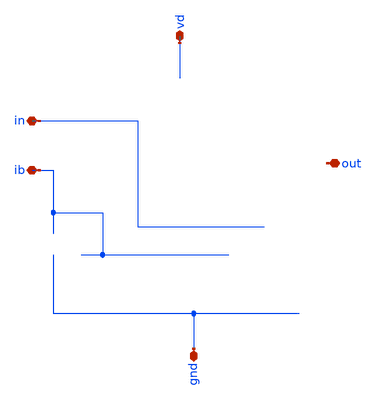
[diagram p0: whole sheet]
** sch_path: buffer/xschem/buffer-pex.sch
* Copyright 2020 Stefan Frederik Schippers
* Licensed under the Apache License, Version 2.0 (the "License");
* you may not use this file except in compliance with the License.
* You may obtain a copy of the License at
* https://www.apache.org/licenses/LICENSE-2.0
* Unless required by applicable law or agreed to in writing, software
* distributed under the License is distributed on an "AS IS" BASIS,
* WITHOUT WARRANTIES OR CONDITIONS OF ANY KIND, either express or implied.
* See the License for the specific language governing permissions and
* limitations under the License.
**.subckt buffer-pex vd ib out in gnd
*.iopin vd
*.iopin ib
*.iopin out
*.iopin in
*.iopin gnd
**** begin user architecture code


* NGSPICE file created from buffer.ext - technology: sky130A

*.subckt buffer vd ib out in gnd
X0 out.t19 net1.t27 gnd.t45 gnd.t7 sky130_fd_pr__nfet_01v8 ad=0.145 pd=1.29 as=0.145 ps=1.29 w=1 l=1
X1 a_19996_3619# a_19796_3522# a_19738_3619# w_19600_3400# sky130_fd_pr__pfet_01v8 ad=0.29 pd=2.58
+ as=0.29 ps=2.58 w=1 l=1
X2 net2.t11 out.t20 net4.t20 gnd.t8 sky130_fd_pr__nfet_01v8 ad=0.145 pd=1.29 as=0.145 ps=1.29 w=1
+ l=1
X3 gnd.t44 net1.t10 net1 gnd.t9 sky130_fd_pr__nfet_01v8 ad=0.145 pd=1.29 as=0.145 ps=1.29 w=1 l=1
X4 net4.t10 in.t0 net3.t11 gnd.t24 sky130_fd_pr__nfet_01v8 ad=0.145 pd=1.29 as=0.145 ps=1.29 w=1 l=1
X5 net3.t1 net3.t0 vd.t21 vd.t20 sky130_fd_pr__pfet_01v8 ad=0.29 pd=2.58 as=0.29 ps=2.58 w=1 l=1
X6 vd.t19 net3.t12 out.t7 vd.t18 sky130_fd_pr__pfet_01v8 ad=0.145 pd=1.29 as=0.29 ps=2.58 w=1 l=1
X7 a_14516_4519# a_14316_4422# a_14258_4519# w_14120_4300# sky130_fd_pr__pfet_01v8 ad=0.29 pd=2.58
+ as=0.29 ps=2.58 w=1 l=1
X8 a_15696_2770# a_15496_2682# a_15438_2770# gnd.t46 sky130_fd_pr__nfet_01v8 ad=0.29 pd=2.58 as=0.29
+ ps=2.58 w=1 l=1
X9 net1.t0 net2.t12 vd.t43 vd.t42 sky130_fd_pr__pfet_01v8 ad=0.145 pd=1.29 as=0.145 ps=1.29 w=1 l=1
X10 net4.t9 in.t1 net3.t10 gnd.t23 sky130_fd_pr__nfet_01v8 ad=0.145 pd=1.29 as=0.29 ps=2.58 w=1 l=1
X11 net2.t10 out.t21 net4.t18 gnd.t5 sky130_fd_pr__nfet_01v8 ad=0.145 pd=1.29 as=0.145 ps=1.29 w=1
+ l=1
X12 gnd.t43 net1.t11 net1 gnd.t8 sky130_fd_pr__nfet_01v8 ad=0.145 pd=1.29 as=0.145 ps=1.29 w=1 l=1
X13 out.t22 net1.t6 sky130_fd_pr__cap_mim_m3_2 l=21 w=21
X14 net1 net1.t19 gnd.t42 gnd.t24 sky130_fd_pr__nfet_01v8 ad=0.145 pd=1.29 as=0.145 ps=1.29 w=1 l=1
X15 gnd.t41 net1.t15 net1.t16 gnd.t5 sky130_fd_pr__nfet_01v8 ad=0.145 pd=1.29 as=0.145 ps=1.29 w=1
+ l=1
X16 a_19996_4519# a_19796_4422# a_19738_4519# w_19600_4300# sky130_fd_pr__pfet_01v8 ad=0.29 pd=2.58
+ as=0.29 ps=2.58 w=1 l=1
X17 net4.t11 out.t23 net2.t9 gnd.t14 sky130_fd_pr__nfet_01v8 ad=0.145 pd=1.29 as=0.145 ps=1.29 w=1
+ l=1
X18 a_14756_1890# a_14556_1802# a_14498_1890# gnd.t1 sky130_fd_pr__nfet_01v8 ad=0.29 pd=2.58 as=0.29
+ ps=2.58 w=1 l=1
X19 net1.t13 net1.t12 gnd.t40 gnd.t23 sky130_fd_pr__nfet_01v8 ad=0.145 pd=1.29 as=0.29 ps=2.58 w=1
+ l=1
X20 net3.t9 in.t2 net4.t8 gnd.t22 sky130_fd_pr__nfet_01v8 ad=0.145 pd=1.29 as=0.145 ps=1.29 w=1 l=1
X21 net3.t8 in.t3 net4.t7 gnd.t21 sky130_fd_pr__nfet_01v8 ad=0.29 pd=2.58 as=0.145 ps=1.29 w=1 l=1
X22 net2.t1 net2.t0 vd.t41 vd.t40 sky130_fd_pr__pfet_01v8 ad=0.29 pd=2.58 as=0.29 ps=2.58 w=1 l=1
X23 vd.t39 net2.t13 net1.t8 vd.t38 sky130_fd_pr__pfet_01v8 ad=0.145 pd=1.29 as=0.29 ps=2.58 w=1 l=1
X24 net4.t14 out.t24 net2.t8 gnd.t11 sky130_fd_pr__nfet_01v8 ad=0.145 pd=1.29 as=0.145 ps=1.29 w=1
+ l=1
X25 net4.t15 out.t25 net2.t7 gnd.t6 sky130_fd_pr__nfet_01v8 ad=0.145 pd=1.29 as=0.145 ps=1.29 w=1
+ l=1
X26 out.t18 net1.t28 gnd.t39 gnd.t14 sky130_fd_pr__nfet_01v8 ad=0.145 pd=1.29 as=0.145 ps=1.29 w=1
+ l=1
X27 vd.t17 net3.t13 out.t9 vd.t16 sky130_fd_pr__pfet_01v8 ad=0.145 pd=1.29 as=0.145 ps=1.29 w=1 l=1
X28 net2.t6 out.t26 net4.t19 gnd.t10 sky130_fd_pr__nfet_01v8 ad=0.145 pd=1.29 as=0.145 ps=1.29 w=1
+ l=1
X29 out.t1 net3.t14 vd.t15 vd.t14 sky130_fd_pr__pfet_01v8 ad=0.145 pd=1.29 as=0.29 ps=2.58 w=1 l=1
X30 net4.t6 in.t4 net3.t7 gnd.t20 sky130_fd_pr__nfet_01v8 ad=0.145 pd=1.29 as=0.145 ps=1.29 w=1 l=1
X31 gnd.t26 net1.t29 out.t17 gnd.t21 sky130_fd_pr__nfet_01v8 ad=0.29 pd=2.58 as=0.145 ps=1.29 w=1
+ l=1
X32 gnd.t38 net1.t30 out.t16 gnd.t22 sky130_fd_pr__nfet_01v8 ad=0.145 pd=1.29 as=0.145 ps=1.29 w=1
+ l=1
X33 gnd.t37 net1.t24 net1.t25 gnd.t10 sky130_fd_pr__nfet_01v8 ad=0.145 pd=1.29 as=0.145 ps=1.29 w=1
+ l=1
X34 out.t15 net1.t31 gnd.t28 gnd.t11 sky130_fd_pr__nfet_01v8 ad=0.145 pd=1.29 as=0.145 ps=1.29 w=1
+ l=1
X35 out.t14 net1.t32 gnd.t36 gnd.t6 sky130_fd_pr__nfet_01v8 ad=0.145 pd=1.29 as=0.145 ps=1.29 w=1
+ l=1
X36 net1.t23 net1.t22 gnd.t35 gnd.t20 sky130_fd_pr__nfet_01v8 ad=0.145 pd=1.29 as=0.145 ps=1.29 w=1
+ l=1
X37 gnd.t13 ib.t0 ib.t1 gnd.t12 sky130_fd_pr__nfet_01v8 ad=0.145 pd=1.29 as=0.29 ps=2.58 w=1 l=1
X38 net4.t0 ib.t2 gnd.t3 gnd.t2 sky130_fd_pr__nfet_01v8 ad=0.29 pd=2.58 as=0.145 ps=1.29 w=1 l=1
X39 vd.t13 net3.t15 out.t8 vd.t12 sky130_fd_pr__pfet_01v8 ad=0.29 pd=2.58 as=0.145 ps=1.29 w=1 l=1
X40 net3.t6 in.t5 net4.t5 gnd.t19 sky130_fd_pr__nfet_01v8 ad=0.145 pd=1.29 as=0.145 ps=1.29 w=1 l=1
X41 vd.t11 net3.t16 out.t6 vd.t10 sky130_fd_pr__pfet_01v8 ad=0.145 pd=1.29 as=0.145 ps=1.29 w=1 l=1
X42 net4.t16 out.t27 net2.t5 gnd.t0 sky130_fd_pr__nfet_01v8 ad=0.145 pd=1.29 as=0.145 ps=1.29 w=1
+ l=1
X43 out.t0 net3.t17 vd.t9 vd.t8 sky130_fd_pr__pfet_01v8 ad=0.145 pd=1.29 as=0.145 ps=1.29 w=1 l=1
X44 vd.t7 net3.t18 out.t3 vd.t6 sky130_fd_pr__pfet_01v8 ad=0.145 pd=1.29 as=0.145 ps=1.29 w=1 l=1
X45 net4.t4 in.t6 net3.t5 gnd.t18 sky130_fd_pr__nfet_01v8 ad=0.145 pd=1.29 as=0.145 ps=1.29 w=1 l=1
X46 net2.t4 out.t28 net4.t12 gnd.t33 sky130_fd_pr__nfet_01v8 ad=0.145 pd=1.29 as=0.145 ps=1.29 w=1
+ l=1
X47 vd.t37 net2.t14 net1.t26 vd.t36 sky130_fd_pr__pfet_01v8 ad=0.145 pd=1.29 as=0.145 ps=1.29 w=1
+ l=1
X48 out.t5 net3.t19 vd.t5 vd.t4 sky130_fd_pr__pfet_01v8 ad=0.29 pd=2.58 as=0.145 ps=1.29 w=1 l=1
X49 out.t2 net3.t20 vd.t3 vd.t2 sky130_fd_pr__pfet_01v8 ad=0.145 pd=1.29 as=0.145 ps=1.29 w=1 l=1
X50 net4.t3 in.t7 net3.t4 gnd.t17 sky130_fd_pr__nfet_01v8 ad=0.145 pd=1.29 as=0.145 ps=1.29 w=1 l=1
X51 net1.t7 net2.t15 vd.t35 vd.t34 sky130_fd_pr__pfet_01v8 ad=0.145 pd=1.29 as=0.29 ps=2.58 w=1 l=1
X52 gnd.t27 net1.t33 out.t13 gnd.t19 sky130_fd_pr__nfet_01v8 ad=0.145 pd=1.29 as=0.145 ps=1.29 w=1
+ l=1
X53 gnd.t34 net1.t20 net1.t21 gnd.t33 sky130_fd_pr__nfet_01v8 ad=0.145 pd=1.29 as=0.145 ps=1.29 w=1
+ l=1
X54 out.t12 net1.t34 gnd.t32 gnd.t0 sky130_fd_pr__nfet_01v8 ad=0.145 pd=1.29 as=0.145 ps=1.29 w=1
+ l=1
X55 a_21836_2770# a_21636_2682# a_21578_2770# gnd.t4 sky130_fd_pr__nfet_01v8 ad=0.29 pd=2.58 as=0.29
+ ps=2.58 w=1 l=1
X56 net1.t18 net1.t17 gnd.t31 gnd.t18 sky130_fd_pr__nfet_01v8 ad=0.145 pd=1.29 as=0.145 ps=1.29 w=1
+ l=1
X57 net1 net1.t14 gnd.t30 gnd.t17 sky130_fd_pr__nfet_01v8 ad=0.145 pd=1.29 as=0.145 ps=1.29 w=1 l=1
X58 a_14516_3619# a_14316_3522# a_14258_3619# w_14120_3400# sky130_fd_pr__pfet_01v8 ad=0.29 pd=2.58
+ as=0.29 ps=2.58 w=1 l=1
X59 net3.t3 in.t8 net4.t2 gnd.t16 sky130_fd_pr__nfet_01v8 ad=0.145 pd=1.29 as=0.145 ps=1.29 w=1 l=1
X60 net3.t2 in.t9 net4.t1 gnd.t15 sky130_fd_pr__nfet_01v8 ad=0.145 pd=1.29 as=0.145 ps=1.29 w=1 l=1
X61 vd.t33 net2.t16 net1.t3 vd.t32 sky130_fd_pr__pfet_01v8 ad=0.29 pd=2.58 as=0.145 ps=1.29 w=1 l=1
X62 out.t4 net3.t21 vd.t1 vd.t0 sky130_fd_pr__pfet_01v8 ad=0.145 pd=1.29 as=0.145 ps=1.29 w=1 l=1
X63 net4.t17 out.t29 net2.t3 gnd.t7 sky130_fd_pr__nfet_01v8 ad=0.145 pd=1.29 as=0.145 ps=1.29 w=1
+ l=1
X64 vd.t31 net2.t17 net1.t4 vd.t30 sky130_fd_pr__pfet_01v8 ad=0.145 pd=1.29 as=0.145 ps=1.29 w=1 l=1
X65 net2.t2 out.t30 net4.t13 gnd.t9 sky130_fd_pr__nfet_01v8 ad=0.145 pd=1.29 as=0.145 ps=1.29 w=1
+ l=1
X66 a_21836_1890# a_21636_1802# a_21578_1890# gnd.t4 sky130_fd_pr__nfet_01v8 ad=0.29 pd=2.58 as=0.29
+ ps=2.58 w=1 l=1
X67 net1.t1 net2.t18 vd.t29 vd.t28 sky130_fd_pr__pfet_01v8 ad=0.145 pd=1.29 as=0.145 ps=1.29 w=1 l=1
X68 net1.t5 net2.t19 vd.t27 vd.t26 sky130_fd_pr__pfet_01v8 ad=0.145 pd=1.29 as=0.145 ps=1.29 w=1 l=1
X69 vd.t25 net2.t20 net1.t2 vd.t24 sky130_fd_pr__pfet_01v8 ad=0.145 pd=1.29 as=0.145 ps=1.29 w=1 l=1
X70 net1.t9 net2.t21 vd.t23 vd.t22 sky130_fd_pr__pfet_01v8 ad=0.29 pd=2.58 as=0.145 ps=1.29 w=1 l=1
X71 gnd.t29 net1.t35 out.t11 gnd.t16 sky130_fd_pr__nfet_01v8 ad=0.145 pd=1.29 as=0.145 ps=1.29 w=1
+ l=1
X72 gnd.t25 net1.t36 out.t10 gnd.t15 sky130_fd_pr__nfet_01v8 ad=0.145 pd=1.29 as=0.145 ps=1.29 w=1
+ l=1
R0 net1.n12 net1.t29 172.22
R1 net1.n13 net1.n12 149.524
R2 net1.n14 net1.n13 149.524
R3 net1.n15 net1.n14 149.524
R4 net1.n16 net1.n15 149.524
R5 net1.n17 net1.n16 149.524
R6 net1.n18 net1.n17 149.524
R7 net1.n19 net1.n18 149.524
R8 net1.n20 net1.n19 149.524
R9 net1.n21 net1.n20 149.524
R10 net1.n22 net1.n21 149.524
R11 net1.n23 net1.n22 149.524
R12 net1.n24 net1.n23 149.524
R13 net1.n25 net1.n24 149.524
R14 net1.n26 net1.n25 149.524
R15 net1.n27 net1.n26 149.524
R16 net1.n28 net1.n27 149.524
R17 net1.n29 net1.n28 149.524
R18 net1.n1 net1.n29 148.639
R19 net1.n10 net1.t9 28.7308
R20 net1.n8 net1.t8 28.7308
R21 net1.n9 net1.t26 28.5655
R22 net1.n9 net1.t7 28.5655
R23 net1.n3 net1.t4 28.5655
R24 net1.n3 net1.t1 28.5655
R25 net1.n7 net1.t3 28.5655
R26 net1.n7 net1.t0 28.5655
R27 net1.n4 net1.t2 28.5655
R28 net1.n4 net1.t5 28.5655
R29 net1.n1 net1.t12 24.2846
R30 net1.n29 net1.t24 24.1012
R31 net1.n28 net1.t31 24.1012
R32 net1.n27 net1.t33 24.1012
R33 net1.n26 net1.t17 24.1012
R34 net1.n25 net1.t20 24.1012
R35 net1.n24 net1.t27 24.1012
R36 net1.n23 net1.t35 24.1012
R37 net1.n22 net1.t22 24.1012
R38 net1.n21 net1.t15 24.1012
R39 net1.n20 net1.t32 24.1012
R40 net1.n19 net1.t30 24.1012
R41 net1.n18 net1.t14 24.1012
R42 net1.n17 net1.t10 24.1012
R43 net1.n16 net1.t34 24.1012
R44 net1.n15 net1.t36 24.1012
R45 net1.n14 net1.t19 24.1012
R46 net1.n13 net1.t11 24.1012
R47 net1.n12 net1.t28 24.1012
R48 net1.n2 net1.t25 17.4005
R49 net1.n2 net1.t13 17.4005
R50 net1.n5 net1.t16 17.4005
R51 net1.n5 net1.t23 17.4005
R52 net1.n6 net1.t21 17.4005
R53 net1.n6 net1.t18 17.4005
R54 net1.n30 net1.n0 3.21925
R55 net1 net1.n30 3.21925
R56 net1.n0 net1.n2 2.85119
R57 net1.n3 net1.n9 2.12411
R58 net1.n4 net1.n7 2.12411
R59 net1.n8 net1.n4 2.12411
R60 net1.n10 net1.n3 2.12411
R61 net1.n2 net1.t6 1.82437
R62 net1.n0 net1.n11 1.56782
R63 net1.n0 net1.n6 1.56492
R64 net1.n2 net1.n1 1.52493
R65 net1.n11 net1.n8 1.00578
R66 net1.n11 net1.n10 0.942223
R67 net1.n30 net1.n5 0.932973
R68 gnd.n3 gnd.n2 12625.4
R69 gnd.n71 gnd.n63 12625.4
R70 gnd.n29 gnd.n28 10965.6
R71 gnd.t11 gnd.n1 10965.6
R72 gnd.n33 gnd.n5 1104.56
R73 gnd.n32 gnd.n27 1104.56
R74 gnd.n33 gnd.n32 1104.56
R75 gnd.n41 gnd.n36 1104.56
R76 gnd.n40 gnd.n38 1104.56
R77 gnd.n41 gnd.n40 1104.56
R78 gnd.t21 gnd.t14 171.897
R79 gnd.t24 gnd.t8 171.897
R80 gnd.t15 gnd.t24 171.897
R81 gnd.t0 gnd.t15 171.897
R82 gnd.t9 gnd.t0 171.897
R83 gnd.t22 gnd.t17 171.897
R84 gnd.t6 gnd.t22 171.897
R85 gnd.t5 gnd.t20 171.897
R86 gnd.t7 gnd.t16 171.897
R87 gnd.t18 gnd.t33 171.897
R88 gnd.t19 gnd.t18 171.897
R89 gnd.t11 gnd.t19 171.897
R90 gnd.t10 gnd.t11 171.897
R91 gnd.t23 gnd.t10 171.897
R92 gnd.t4 gnd.n10 161.903
R93 gnd.n23 gnd.t4 161.903
R94 gnd.n43 gnd.t23 161.903
R95 gnd.t1 gnd.n68 161.903
R96 gnd.n25 gnd.n24 136.584
R97 gnd.n71 gnd.t1 126.591
R98 gnd.n3 gnd.t7 118.596
R99 gnd.n62 gnd.n49 109.317
R100 gnd.n78 gnd.n77 108.424
R101 gnd.t17 gnd.n29 106.603
R102 gnd.n46 gnd.n43 89.2797
R103 gnd.n75 gnd.n74 89.2797
R104 gnd.n25 gnd.n23 87.9472
R105 gnd.n30 gnd.t6 85.9484
R106 gnd.n30 gnd.t5 85.9484
R107 gnd.n59 gnd.t2 85.9484
R108 gnd.n29 gnd.t9 65.2943
R109 gnd.t33 gnd.n3 53.3015
R110 gnd.n56 gnd.t12 51.3027
R111 gnd.n47 gnd.n46 41.3088
R112 gnd.t2 gnd.t46 41.3088
R113 gnd.n74 gnd.n71 35.3124
R114 gnd.n59 gnd.n56 34.6462
R115 gnd.n24 gnd.t21 25.3185
R116 gnd.n85 gnd.t26 20.261
R117 gnd.n98 gnd.t40 17.405
R118 gnd.n0 gnd.t3 17.4005
R119 gnd.n0 gnd.t13 17.4005
R120 gnd.n80 gnd.t28 17.4005
R121 gnd.n80 gnd.t37 17.4005
R122 gnd.n95 gnd.t31 17.4005
R123 gnd.n95 gnd.t27 17.4005
R124 gnd.n81 gnd.t45 17.4005
R125 gnd.n81 gnd.t34 17.4005
R126 gnd.n92 gnd.t35 17.4005
R127 gnd.n92 gnd.t29 17.4005
R128 gnd.n82 gnd.t36 17.4005
R129 gnd.n82 gnd.t41 17.4005
R130 gnd.n89 gnd.t30 17.4005
R131 gnd.n89 gnd.t38 17.4005
R132 gnd.n83 gnd.t32 17.4005
R133 gnd.n83 gnd.t44 17.4005
R134 gnd.n86 gnd.t42 17.4005
R135 gnd.n86 gnd.t25 17.4005
R136 gnd.n84 gnd.t39 17.4005
R137 gnd.n84 gnd.t43 17.4005
R138 gnd.n90 gnd.n88 2.91898
R139 gnd.n93 gnd.n91 2.91898
R140 gnd.n96 gnd.n94 2.90766
R141 gnd.n87 gnd.n85 2.90766
R142 gnd.n98 gnd.n97 2.89724
R143 gnd.n91 gnd.n90 2.88773
R144 gnd.n97 gnd.n96 2.85648
R145 gnd.n88 gnd.n87 2.81391
R146 gnd.n94 gnd.n93 2.81391
R147 gnd gnd.n98 1.09175
R148 gnd gnd.n79 1.063
R149 gnd.n79 gnd.n78 0.884538
R150 gnd.n79 gnd.n0 0.68415
R151 gnd.n16 gnd.n15 0.0464978
R152 gnd.t4 gnd.n16 0.0464978
R153 gnd.n14 gnd.n13 0.0464978
R154 gnd.t4 gnd.n14 0.0464978
R155 gnd.n65 gnd.n64 0.0464978
R156 gnd.t1 gnd.n65 0.0464978
R157 gnd.n70 gnd.n69 0.0464978
R158 gnd.t1 gnd.n70 0.0464978
R159 gnd.n12 gnd.n11 0.0464978
R160 gnd.t4 gnd.n12 0.0464978
R161 gnd.n18 gnd.n17 0.0464978
R162 gnd.t4 gnd.n18 0.0464978
R163 gnd.n51 gnd.n50 0.0464978
R164 gnd.t46 gnd.n51 0.0464978
R165 gnd.n53 gnd.n52 0.0464978
R166 gnd.t46 gnd.n53 0.0464978
R167 gnd.n22 gnd.n21 0.0425017
R168 gnd.n23 gnd.n22 0.0425017
R169 gnd.n7 gnd.n6 0.0425017
R170 gnd.n10 gnd.n7 0.0425017
R171 gnd.n42 gnd.n41 0.0425017
R172 gnd.n43 gnd.n42 0.0425017
R173 gnd.n38 gnd.n37 0.0425017
R174 gnd.n67 gnd.n66 0.0425017
R175 gnd.n68 gnd.n67 0.0425017
R176 gnd.n73 gnd.n72 0.0425017
R177 gnd.n74 gnd.n73 0.0425017
R178 gnd.n20 gnd.n19 0.0425017
R179 gnd.n23 gnd.n20 0.0425017
R180 gnd.n9 gnd.n8 0.0425017
R181 gnd.n10 gnd.n9 0.0425017
R182 gnd.n34 gnd.n33 0.0425017
R183 gnd.n43 gnd.n34 0.0425017
R184 gnd.n27 gnd.n26 0.0425017
R185 gnd.n26 gnd.n25 0.0425017
R186 gnd.n55 gnd.n54 0.0425017
R187 gnd.n56 gnd.n55 0.0425017
R188 gnd.n45 gnd.n44 0.0425017
R189 gnd.n46 gnd.n45 0.0425017
R190 gnd.n49 gnd.n48 0.0425017
R191 gnd.n48 gnd.n47 0.0425017
R192 gnd.n77 gnd.n76 0.0425017
R193 gnd.n76 gnd.n75 0.0425017
R194 gnd.n58 gnd.n57 0.0250016
R195 gnd.n59 gnd.n58 0.0250016
R196 gnd.n79 gnd.n62 0.0147449
R197 gnd.n97 gnd.n80 0.00498379
R198 gnd.n96 gnd.n95 0.00498379
R199 gnd.n94 gnd.n81 0.00498379
R200 gnd.n93 gnd.n92 0.00498379
R201 gnd.n91 gnd.n82 0.00498379
R202 gnd.n90 gnd.n89 0.00498379
R203 gnd.n88 gnd.n83 0.00498379
R204 gnd.n87 gnd.n86 0.00498379
R205 gnd.n85 gnd.n84 0.00498379
R206 gnd.n40 gnd.n39 0.00310298
R207 gnd.n36 gnd.n35 0.00310298
R208 gnd.n32 gnd.n31 0.00310298
R209 gnd.n31 gnd.n30 0.00310298
R210 gnd.n5 gnd.n4 0.00310298
R211 gnd.n62 gnd.n61 0.00137759
R212 gnd.n61 gnd.n60 0.00126683
R213 gnd.n60 gnd.n59 0.00126683
R214 out.t23 out.n17 175.093
R215 out.n8 out.t26 175.046
R216 out.n12 out.n11 150.493
R217 out.n14 out.n13 150.493
R218 out.n16 out.n15 141.107
R219 out.n7 out.t5 28.7308
R220 out.n3 out.t7 28.7308
R221 out.n4 out.t9 28.5655
R222 out.n4 out.t1 28.5655
R223 out.n5 out.t6 28.5655
R224 out.n5 out.t0 28.5655
R225 out.n0 out.t8 28.5655
R226 out.n0 out.t4 28.5655
R227 out.n1 out.t3 28.5655
R228 out.n1 out.t2 28.5655
R229 out.n27 out.t23 26.7906
R230 out.n15 out.t30 24.1039
R231 out.n16 out.t27 24.1036
R232 out.n14 out.t25 24.1032
R233 out.n12 out.t29 24.1029
R234 out.n8 out.t24 24.1029
R235 out.n11 out.t28 24.1029
R236 out.n13 out.t21 24.1029
R237 out.n17 out.t20 24.1029
R238 out.n22 out.t13 17.4005
R239 out.n22 out.t15 17.4005
R240 out.n21 out.t11 17.4005
R241 out.n21 out.t19 17.4005
R242 out.n20 out.t16 17.4005
R243 out.n20 out.t14 17.4005
R244 out.n19 out.t10 17.4005
R245 out.n19 out.t12 17.4005
R246 out.n18 out.t17 17.4005
R247 out.n18 out.t18 17.4005
R248 out out.t22 5.44766
R249 out.n23 out.n22 4.15172
R250 out.n25 out.n24 3.2505
R251 out.n26 out.n25 3.21925
R252 out.n24 out.n23 3.21925
R253 out.n2 out.n0 2.13078
R254 out.n6 out.n4 2.12411
R255 out out.n27 2.00902
R256 out.n7 out.n6 1.95883
R257 out.n3 out.n2 1.95883
R258 out.n10 out.n3 1.71069
R259 out.n9 out.n7 1.40585
R260 out.n27 out.n26 1.28175
R261 out.n17 out.n16 1.08827
R262 out.n13 out.n12 0.990679
R263 out.n23 out.n21 0.932973
R264 out.n25 out.n19 0.932973
R265 out.n26 out.n18 0.932973
R266 out.n24 out.n20 0.92165
R267 out.n15 out.n14 0.915308
R268 out.n10 out.n9 0.8385
R269 out.n6 out.n5 0.165773
R270 out.n2 out.n1 0.165773
R271 out.n9 out.n8 0.0155771
R272 out.n11 out.n10 0.0136023
R273 net4 net4.t0 18.5925
R274 net4.n0 net4.t19 17.4005
R275 net4.n0 net4.t9 17.4005
R276 net4.n1 net4.t5 17.4005
R277 net4.n1 net4.t14 17.4005
R278 net4.n2 net4.t12 17.4005
R279 net4.n2 net4.t4 17.4005
R280 net4.n3 net4.t2 17.4005
R281 net4.n3 net4.t17 17.4005
R282 net4.n4 net4.t18 17.4005
R283 net4.n4 net4.t6 17.4005
R284 net4.n5 net4.t8 17.4005
R285 net4.n5 net4.t15 17.4005
R286 net4.n6 net4.t13 17.4005
R287 net4.n6 net4.t3 17.4005
R288 net4.n7 net4.t1 17.4005
R289 net4.n7 net4.t16 17.4005
R290 net4.n8 net4.t20 17.4005
R291 net4.n8 net4.t10 17.4005
R292 net4.n9 net4.t7 17.4005
R293 net4.n9 net4.t11 17.4005
R294 net4 net4.n0 3.41717
R295 net4.n8 net4.n9 2.86096
R296 net4.n6 net4.n7 2.85648
R297 net4.n1 net4.n2 2.85648
R298 net4.n0 net4.n1 2.85412
R299 net4.n5 net4.n6 2.84964
R300 net4.n2 net4.n3 2.83922
R301 net4.n7 net4.n8 2.8342
R302 net4.n4 net4.n5 2.81839
R303 net4.n3 net4.n4 2.81246
R304 net2.n4 net2.t15 40.0371
R305 net2.n0 net2.t16 40.0371
R306 net2.n8 net2.t0 39.5292
R307 net2.n7 net2.t21 39.5292
R308 net2.n6 net2.t17 39.5292
R309 net2.n5 net2.t18 39.5292
R310 net2.n4 net2.t14 39.5292
R311 net2.n3 net2.t13 39.5292
R312 net2.n2 net2.t19 39.5292
R313 net2.n1 net2.t20 39.5292
R314 net2.n0 net2.t12 39.5292
R315 net2.n10 net2.t1 28.5701
R316 net2.n18 net2.t8 17.4005
R317 net2.n18 net2.t6 17.4005
R318 net2.n11 net2.t3 17.4005
R319 net2.n11 net2.t4 17.4005
R320 net2.n13 net2.t5 17.4005
R321 net2.n13 net2.t2 17.4005
R322 net2.n12 net2.t7 17.4005
R323 net2.n12 net2.t10 17.4005
R324 net2.n14 net2.t9 17.4005
R325 net2.n14 net2.t11 17.4005
R326 net2.n15 net2.n14 3.31748
R327 net2.n17 net2.n16 2.58608
R328 net2.n16 net2.n15 2.5755
R329 net2.n19 net2.n18 2.45901
R330 net2.n8 net2.n7 1.98336
R331 net2.n9 net2.n3 1.70943
R332 net2 net2.n19 1.51695
R333 net2 net2.n10 0.988132
R334 net2.n15 net2.n13 0.742484
R335 net2.n16 net2.n12 0.737582
R336 net2.n17 net2.n11 0.690833
R337 net2.n19 net2.n17 0.662313
R338 net2.n5 net2.n4 0.508357
R339 net2.n6 net2.n5 0.508357
R340 net2.n7 net2.n6 0.508357
R341 net2.n1 net2.n0 0.508357
R342 net2.n2 net2.n1 0.508357
R343 net2.n3 net2.n2 0.508357
R344 net2.n10 net2.n9 0.336824
R345 net2.n9 net2.n8 0.304429
R346 in.n1 in.n0 150.876
R347 in.n5 in.n4 150.492
R348 in.n3 in.n2 150.489
R349 in.n7 in.n6 141.162
R350 in.n0 in.t3 25.2315
R351 in.n6 in.t6 24.1052
R352 in.n0 in.t0 24.1044
R353 in.n2 in.t7 24.1037
R354 in.n4 in.t4 24.103
R355 in.n1 in.t9 24.1029
R356 in.n5 in.t8 24.1029
R357 in.n3 in.t2 24.1029
R358 in.n7 in.t5 24.1029
R359 in.n9 in.t1 24.1005
R360 in.n14 in.n13 9.3005
R361 in in.n14 8.35727
R362 in.n8 in.n7 1.7896
R363 in.n2 in.n1 1.10484
R364 in.n4 in.n3 1.09917
R365 in.n6 in.n5 0.414445
R366 in.n14 in.n12 0.0775833
R367 in.n12 in.n8 0.0145625
R368 in.n12 in.n11 0.00561551
R369 in.n10 in.n9 0.00553045
R370 in.n11 in.n10 0.00113271
R371 net3.n13 net3.t14 40.108
R372 net3.n9 net3.t15 40.108
R373 net3.n17 net3.t0 39.5292
R374 net3.n16 net3.t19 39.5292
R375 net3.n15 net3.t16 39.5292
R376 net3.n14 net3.t17 39.5292
R377 net3.n13 net3.t13 39.5292
R378 net3.n12 net3.t12 39.5292
R379 net3.n11 net3.t20 39.5292
R380 net3.n10 net3.t18 39.5292
R381 net3.n9 net3.t21 39.5292
R382 net3.n18 net3.t1 29.0347
R383 net3.n7 net3.t10 21.5322
R384 net3.n3 net3.t8 21.5205
R385 net3.n6 net3.t5 17.4005
R386 net3.n6 net3.t6 17.4005
R387 net3.n0 net3.t7 17.4005
R388 net3.n0 net3.t3 17.4005
R389 net3.n1 net3.t4 17.4005
R390 net3.n1 net3.t9 17.4005
R391 net3.n2 net3.t11 17.4005
R392 net3.n2 net3.t2 17.4005
R393 net3.n4 net3.n3 3.2505
R394 net3.n5 net3.n4 3.21925
R395 net3.n17 net3.n16 2.05429
R396 net3 net3.n18 1.83383
R397 net3.n18 net3.n12 1.7699
R398 net3.n8 net3.n5 1.65675
R399 net3.n8 net3.n7 1.563
R400 net3.n7 net3.n6 0.901723
R401 net3.n5 net3.n0 0.901723
R402 net3.n4 net3.n1 0.901723
R403 net3.n3 net3.n2 0.892665
R404 net3 net3.n8 0.688
R405 net3.n14 net3.n13 0.579293
R406 net3.n15 net3.n14 0.579293
R407 net3.n16 net3.n15 0.579293
R408 net3.n10 net3.n9 0.579293
R409 net3.n11 net3.n10 0.579293
R410 net3.n12 net3.n11 0.579293
R411 net3.n18 net3.n17 0.314897
R412 vd.t6 vd.t0 384.17
R413 vd.t6 vd.t2 384.17
R414 vd.t24 vd.t42 384.17
R415 vd.t24 vd.t26 384.17
R416 vd.t8 vd.t10 384.17
R417 vd.t8 vd.t16 384.17
R418 vd.t28 vd.t30 384.17
R419 vd.t28 vd.t36 384.17
R420 vd.n94 vd.n93 379.483
R421 vd.n78 vd.n74 379.483
R422 vd.n92 vd.t18 361.846
R423 vd.n73 vd.t38 361.846
R424 vd.n53 vd.t4 361.846
R425 vd.n60 vd.t14 361.846
R426 vd.n21 vd.t22 361.846
R427 vd.n28 vd.t34 361.846
R428 vd.n85 vd.t12 361.836
R429 vd.n70 vd.t32 361.836
R430 vd.n95 vd.n94 297.413
R431 vd.n79 vd.n78 297.413
R432 vd.n38 vd.n33 185.225
R433 vd.n6 vd.n1 185.225
R434 vd.n39 vd.n38 131.012
R435 vd.n7 vd.n6 131.012
R436 vd.n59 vd.n54 113.749
R437 vd.n27 vd.n22 113.749
R438 vd.n62 vd.n61 111.812
R439 vd.n30 vd.n29 111.812
R440 vd.n98 vd.t21 29.658
R441 vd.n98 vd.t41 29.6205
R442 vd.n84 vd.t13 28.7468
R443 vd.n67 vd.t33 28.7468
R444 vd.n52 vd.t15 28.706
R445 vd.n20 vd.t35 28.5837
R446 vd.n81 vd.t3 28.5655
R447 vd.n81 vd.t19 28.5655
R448 vd.n82 vd.t1 28.5655
R449 vd.n82 vd.t7 28.5655
R450 vd.n64 vd.t27 28.5655
R451 vd.n64 vd.t39 28.5655
R452 vd.n65 vd.t43 28.5655
R453 vd.n65 vd.t25 28.5655
R454 vd.n48 vd.t5 28.5655
R455 vd.n48 vd.t11 28.5655
R456 vd.n50 vd.t9 28.5655
R457 vd.n50 vd.t17 28.5655
R458 vd.n16 vd.t23 28.5655
R459 vd.n16 vd.t31 28.5655
R460 vd.n18 vd.t29 28.5655
R461 vd.n18 vd.t37 28.5655
R462 vd.n49 vd.n47 3.12941
R463 vd.n17 vd.n15 3.12941
R464 vd.n98 vd.n97 2.23127
R465 vd.n83 vd.n81 2.14011
R466 vd.n66 vd.n64 2.14011
R467 vd.n20 vd.n19 2.08383
R468 vd.n52 vd.n51 2.05467
R469 vd.n84 vd.n83 1.95883
R470 vd.n67 vd.n66 1.95883
R471 vd.n51 vd.n49 1.95883
R472 vd.n19 vd.n17 1.95883
R473 vd.n63 vd.n59 1.80001
R474 vd.n31 vd.n27 1.80001
R475 vd.n99 vd.n98 1.79858
R476 vd vd.n99 1.20242
R477 vd.n31 vd.n20 0.823417
R478 vd.n63 vd.n52 0.483833
R479 vd.n69 vd.n68 0.324076
R480 vd.n99 vd.n63 0.31925
R481 vd.n99 vd.n31 0.28175
R482 vd.n88 vd.n84 0.2505
R483 vd.n69 vd.n67 0.2505
R484 vd.n80 vd.n72 0.227583
R485 vd.n83 vd.n82 0.181781
R486 vd.n66 vd.n65 0.181781
R487 vd.n49 vd.n48 0.181781
R488 vd.n51 vd.n50 0.181781
R489 vd.n17 vd.n16 0.181781
R490 vd.n19 vd.n18 0.181781
R491 vd.n97 vd.n96 0.180708
R492 vd.n88 vd.n87 0.169709
R493 vd.n97 vd.n80 0.168208
R494 vd.n45 vd.n40 0.162238
R495 vd.n13 vd.n8 0.162238
R496 vd.n43 vd.n42 0.162231
R497 vd.n11 vd.n10 0.162231
R498 vd.n42 vd.n41 0.16179
R499 vd.n40 vd.n39 0.16179
R500 vd.n10 vd.n9 0.16179
R501 vd.n8 vd.n7 0.16179
R502 vd.n63 vd.n62 0.150843
R503 vd.n31 vd.n30 0.150843
R504 vd.n96 vd.n88 0.127583
R505 vd.n72 vd.n69 0.1005
R506 vd.n80 vd.n79 0.0176904
R507 vd.n96 vd.n95 0.0176904
R508 vd.n35 vd.n34 0.0150463
R509 vd.t20 vd.n35 0.0150463
R510 vd.n38 vd.n37 0.0150463
R511 vd.n3 vd.n2 0.0150463
R512 vd.t40 vd.n3 0.0150463
R513 vd.n6 vd.n5 0.0150463
R514 vd.n93 vd.n92 0.0130799
R515 vd.n74 vd.n73 0.0130799
R516 vd.n33 vd.n32 0.0130799
R517 vd.n61 vd.n60 0.0130799
R518 vd.n54 vd.n53 0.0130799
R519 vd.n1 vd.n0 0.0130799
R520 vd.n22 vd.n21 0.0130799
R521 vd.n29 vd.n28 0.0130799
R522 vd.n37 vd.n36 0.0130378
R523 vd.n5 vd.n4 0.0130378
R524 vd.n94 vd.n91 0.00372558
R525 vd.n91 vd.t6 0.00372558
R526 vd.n90 vd.n89 0.00372558
R527 vd.t6 vd.n90 0.00372558
R528 vd.n76 vd.n75 0.00372558
R529 vd.t24 vd.n76 0.00372558
R530 vd.n78 vd.n77 0.00372558
R531 vd.n77 vd.t24 0.00372558
R532 vd.n56 vd.n55 0.00372558
R533 vd.t8 vd.n56 0.00372558
R534 vd.n24 vd.n23 0.00372558
R535 vd.t28 vd.n24 0.00372558
R536 vd.n46 vd.n45 0.00358969
R537 vd.n14 vd.n13 0.00358969
R538 vd.n36 vd.t20 0.00350844
R539 vd.n4 vd.t40 0.00350844
R540 vd.n47 vd.n46 0.0028487
R541 vd.n15 vd.n14 0.0028487
R542 vd.n86 vd.n85 0.00170425
R543 vd.n71 vd.n70 0.00170425
R544 vd.n87 vd.n86 0.0015662
R545 vd.n59 vd.n58 0.00116495
R546 vd.n27 vd.n26 0.00116248
R547 vd.n72 vd.n71 0.00107041
R548 vd.n44 vd.n43 0.00100804
R549 vd.n12 vd.n11 0.00100804
R550 vd.n45 vd.n44 0.00100082
R551 vd.n13 vd.n12 0.00100082
R552 vd.n58 vd.n57 0.000808779
R553 vd.n57 vd.t8 0.000808779
R554 vd.n25 vd.t28 0.000808779
R555 vd.n26 vd.n25 0.000808779
R556 ib.n0 ib.t2 24.8402
R557 ib.n0 ib.t0 24.1079
R558 ib.n1 ib.t1 17.7487
R559 ib ib.n1 4.15675
R560 ib.n1 ib.n0 0.388521
C0 out net3 2.36f
C1 net3 net1 0.16f
C2 in ib 0.0824f
C3 net3 in 1.33f
C4 net4 ib 0.078f
C5 w_19600_4300# a_19796_4422# 0.395f
C6 a_21578_2770# a_21836_2770# 0.0212f
C7 net3 net4 2.05f
C8 a_14756_1890# a_14498_1890# 0.0212f
C9 a_14516_3619# a_14258_3619# 0.0212f
C10 out net1 37.2f
C11 a_19796_3522# net3 0.0141f
C12 a_14516_3619# w_14120_3400# 0.0649f
C13 vd w_14120_4300# 0.123f
C14 w_19600_4300# a_19996_4519# 0.0649f
C15 out in 2.54f
C16 a_14516_4519# w_14120_4300# 0.0649f
C17 net3 w_19600_3400# 0.0399f
C18 net1 in 0.296f
C19 a_15496_2682# in 0.102f
C20 out a_21636_1802# 0.0539f
C21 a_14258_4519# w_14120_4300# 0.0649f
C22 out net4 2.68f
C23 net1 net4 0.0315f
C24 in a_15696_2770# 0.0215f
C25 net2 vd 7.73f
C26 a_19796_3522# out 0.0116f
C27 w_14120_3400# w_14120_4300# 0.0394f
C28 in net4 2.7f
C29 w_14120_4300# a_14316_4422# 0.395f
C30 out w_19600_3400# 0.0264f
C31 vd a_14316_3522# 0.0215f
C32 a_19738_4519# a_19996_4519# 0.0212f
C33 a_14516_4519# a_14258_4519# 0.0212f
C34 a_19738_3619# w_19600_3400# 0.0649f
C35 w_19600_3400# in 0.0115f
C36 vd w_14120_3400# 0.116f
C37 vd a_14316_4422# 0.0237f
C38 vd a_19796_4422# 0.0104f
C39 w_14120_3400# a_14316_3522# 0.395f
C40 a_19796_3522# w_19600_3400# 0.395f
C41 w_19600_3400# w_19600_4300# 0.0394f
C42 a_14258_3619# w_14120_3400# 0.0649f
C43 vd net3 7.02f
C44 net2 net3 0.338f
C45 a_19738_3619# a_19996_3619# 0.0212f
C46 a_21836_1890# a_21578_1890# 0.0212f
C47 w_19600_4300# a_19738_4519# 0.0649f
C48 vd out 1.65f
C49 vd net1 2.07f
C50 net2 out 2.31f
C51 net2 net1 2.15f
C52 a_15438_2770# a_15696_2770# 0.0212f
C53 ib a_14556_1802# 0.0355f
C54 a_19996_3619# w_19600_3400# 0.0649f
C55 vd in 0.16f
C56 net2 in 0.615f
C57 a_21636_2682# in 0.0102f
C58 net2 net4 1.87f
C59 a_14316_3522# in 0.01f
C60 vd w_19600_4300# 0.0724f
C61 w_14120_3400# in 0.0401f
C62 vd w_19600_3400# 0.0714f
*.ends



**** end user architecture code
**.ends
.end
